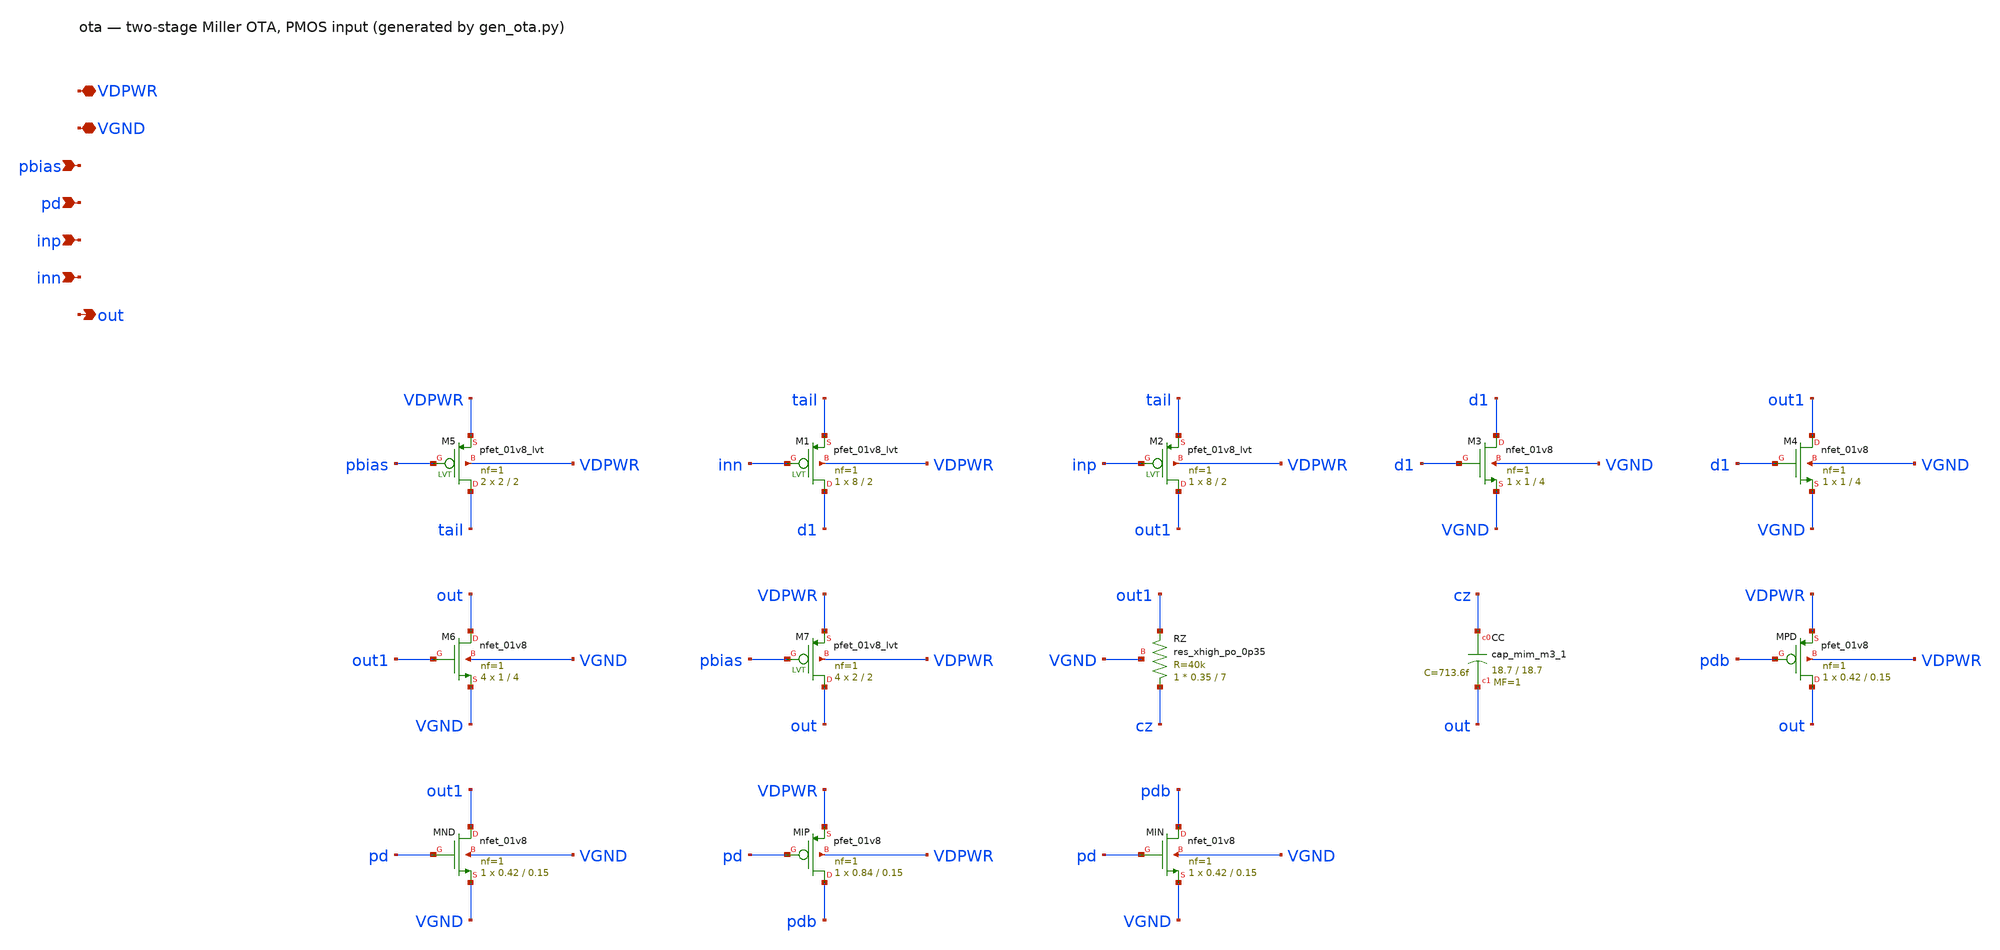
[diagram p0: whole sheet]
** sch_path: xschem/ota.sch
**.subckt ota VDPWR VGND pbias pd inp inn out
*.iopin VDPWR
*.iopin VGND
*.ipin pbias
*.ipin pd
*.ipin inp
*.ipin inn
*.opin out
XM5 tail pbias VDPWR VDPWR sky130_fd_pr__pfet_01v8_lvt L=2 W=2 nf=1 ad='int((1 + 1)/2) * 2 / 1 * 0.29'
+ as='int((1 + 2)/2) * 2 / 1 * 0.29' pd='2*int((1 + 1)/2) * (2 / 1 + 0.29)' ps='2*int((1 + 2)/2) * (2 / 1 + 0.29)'
+ nrd='0.29 / 2 ' nrs='0.29 / 2 ' sa=0 sb=0 sd=0 mult=2 m=2
XM1 d1 inn tail VDPWR sky130_fd_pr__pfet_01v8_lvt L=2 W=8 nf=1 ad='int((1 + 1)/2) * 8 / 1 * 0.29' as='int((1 + 2)/2) * 8 / 1 * 0.29'
+ pd='2*int((1 + 1)/2) * (8 / 1 + 0.29)' ps='2*int((1 + 2)/2) * (8 / 1 + 0.29)' nrd='0.29 / 8 ' nrs='0.29 / 8 '
+ sa=0 sb=0 sd=0 mult=1 m=1
XM2 out1 inp tail VDPWR sky130_fd_pr__pfet_01v8_lvt L=2 W=8 nf=1 ad='int((1 + 1)/2) * 8 / 1 * 0.29' as='int((1 + 2)/2) * 8 / 1 * 0.29'
+ pd='2*int((1 + 1)/2) * (8 / 1 + 0.29)' ps='2*int((1 + 2)/2) * (8 / 1 + 0.29)' nrd='0.29 / 8 ' nrs='0.29 / 8 '
+ sa=0 sb=0 sd=0 mult=1 m=1
XM3 d1 d1 VGND VGND sky130_fd_pr__nfet_01v8 L=4 W=1 nf=1 ad='int((1 + 1)/2) * 1 / 1 * 0.29' as='int((1 + 2)/2) * 1 / 1 * 0.29'
+ pd='2*int((1 + 1)/2) * (1 / 1 + 0.29)' ps='2*int((1 + 2)/2) * (1 / 1 + 0.29)' nrd='0.29 / 1 ' nrs='0.29 / 1 '
+ sa=0 sb=0 sd=0 mult=1 m=1
XM4 out1 d1 VGND VGND sky130_fd_pr__nfet_01v8 L=4 W=1 nf=1 ad='int((1 + 1)/2) * 1 / 1 * 0.29' as='int((1 + 2)/2) * 1 / 1 * 0.29'
+ pd='2*int((1 + 1)/2) * (1 / 1 + 0.29)' ps='2*int((1 + 2)/2) * (1 / 1 + 0.29)' nrd='0.29 / 1 ' nrs='0.29 / 1 '
+ sa=0 sb=0 sd=0 mult=1 m=1
XM6 out out1 VGND VGND sky130_fd_pr__nfet_01v8 L=4 W=1 nf=1 ad='int((1 + 1)/2) * 1 / 1 * 0.29' as='int((1 + 2)/2) * 1 / 1 * 0.29'
+ pd='2*int((1 + 1)/2) * (1 / 1 + 0.29)' ps='2*int((1 + 2)/2) * (1 / 1 + 0.29)' nrd='0.29 / 1 ' nrs='0.29 / 1 '
+ sa=0 sb=0 sd=0 mult=4 m=4
XM7 out pbias VDPWR VDPWR sky130_fd_pr__pfet_01v8_lvt L=2 W=2 nf=1 ad='int((1 + 1)/2) * 2 / 1 * 0.29'
+ as='int((1 + 2)/2) * 2 / 1 * 0.29' pd='2*int((1 + 1)/2) * (2 / 1 + 0.29)' ps='2*int((1 + 2)/2) * (2 / 1 + 0.29)'
+ nrd='0.29 / 2 ' nrs='0.29 / 2 ' sa=0 sb=0 sd=0 mult=4 m=4
XRZ cz out1 VGND sky130_fd_pr__res_xhigh_po_0p35 L=7 mult=1 m=1
XCC cz out sky130_fd_pr__cap_mim_m3_1 W=18.7 L=18.7 MF=1 m=1
XMPD out pdb VDPWR VDPWR sky130_fd_pr__pfet_01v8 L=0.15 W=0.42 nf=1 ad='int((nf+1)/2) * W/nf * 0.29'
+ as='int((nf+2)/2) * W/nf * 0.29' pd='2*int((nf+1)/2) * (W/nf + 0.29)' ps='2*int((nf+2)/2) * (W/nf + 0.29)'
+ nrd='0.29 / W' nrs='0.29 / W' sa=0 sb=0 sd=0 mult=1 m=1
XMND out1 pd VGND VGND sky130_fd_pr__nfet_01v8 L=0.15 W=0.42 nf=1 ad='int((1 + 1)/2) * 0.42 / 1 * 0.29'
+ as='int((1 + 2)/2) * 0.42 / 1 * 0.29' pd='2*int((1 + 1)/2) * (0.42 / 1 + 0.29)' ps='2*int((1 + 2)/2) * (0.42 / 1 + 0.29)'
+ nrd='0.29 / 0.42 ' nrs='0.29 / 0.42 ' sa=0 sb=0 sd=0 mult=1 m=1
XMIP pdb pd VDPWR VDPWR sky130_fd_pr__pfet_01v8 L=0.15 W=0.84 nf=1 ad='int((nf+1)/2) * W/nf * 0.29' as='int((nf+2)/2) * W/nf * 0.29'
+ pd='2*int((nf+1)/2) * (W/nf + 0.29)' ps='2*int((nf+2)/2) * (W/nf + 0.29)' nrd='0.29 / W' nrs='0.29 / W'
+ sa=0 sb=0 sd=0 mult=1 m=1
XMIN pdb pd VGND VGND sky130_fd_pr__nfet_01v8 L=0.15 W=0.42 nf=1 ad='int((1 + 1)/2) * 0.42 / 1 * 0.29'
+ as='int((1 + 2)/2) * 0.42 / 1 * 0.29' pd='2*int((1 + 1)/2) * (0.42 / 1 + 0.29)' ps='2*int((1 + 2)/2) * (0.42 / 1 + 0.29)'
+ nrd='0.29 / 0.42 ' nrs='0.29 / 0.42 ' sa=0 sb=0 sd=0 mult=1 m=1
**.ends
.end
